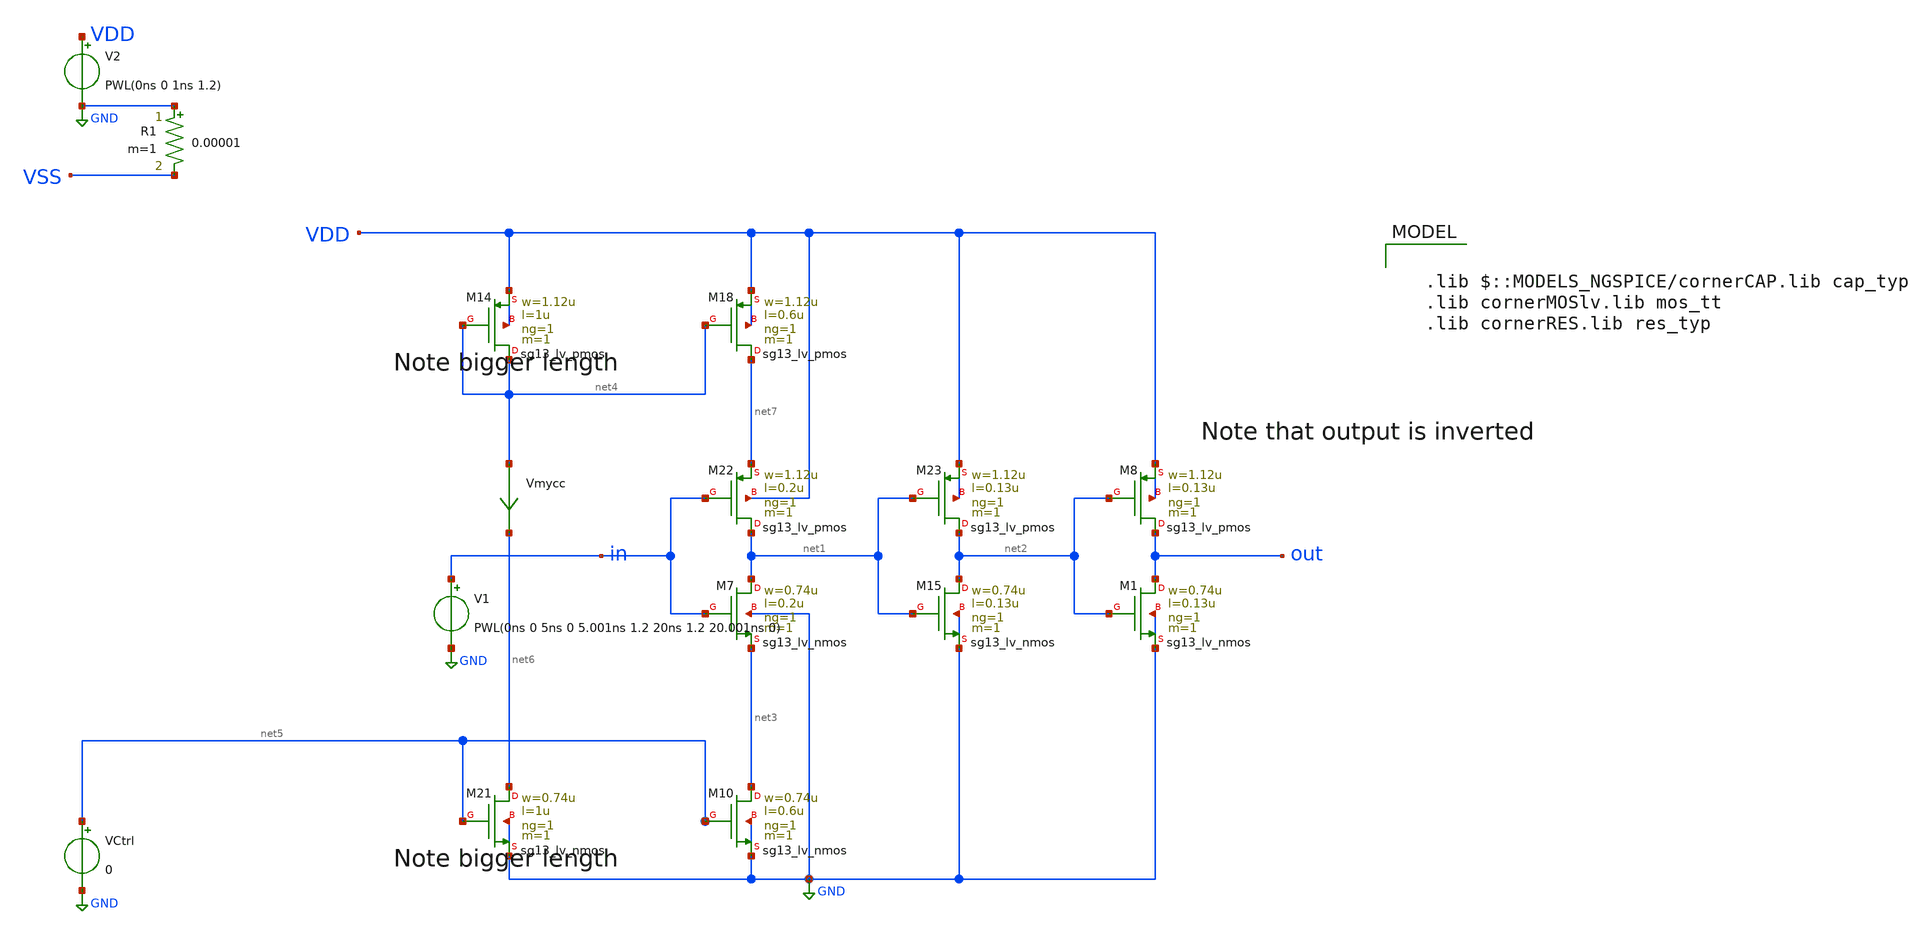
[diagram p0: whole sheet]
** sch_path: schematics/wip/delay_line_vary_voltage.sch
**.subckt delay_line_vary_voltage
XM7 net1 in net3 GND sg13_lv_nmos w=0.74u l=0.2u ng=1 m=1 mm_ok=1
XM10 net3 net5 GND GND sg13_lv_nmos w=0.74u l=0.6u ng=1 m=1 mm_ok=1
Vmycc net4 net6 0
.save i(vmycc)
XM18 net7 net4 VDD VDD sg13_lv_pmos w=1.12u l=0.6u ng=1 m=1 mm_ok=1
XM14 net4 net4 VDD VDD sg13_lv_pmos w=1.12u l=1u ng=1 m=1 mm_ok=1
XM15 net2 net1 GND GND sg13_lv_nmos w=0.74u l=0.13u ng=1 m=1 mm_ok=1
XM21 net6 net5 GND GND sg13_lv_nmos w=0.74u l=1u ng=1 m=1 mm_ok=1
XM22 net1 in net7 VDD sg13_lv_pmos w=1.12u l=0.2u ng=1 m=1 mm_ok=1
XM23 net2 net1 VDD VDD sg13_lv_pmos w=1.12u l=0.13u ng=1 m=1 mm_ok=1
V2 VDD GND PWL(0ns 0 1ns 1.2)
V1 in GND PWL(0ns 0 5ns 0 5.001ns 1.2 20ns 1.2 20.001ns 0)
R1 GND VSS 0.00001 m=1
VCtrl net5 GND 0
XM1 out net2 GND GND sg13_lv_nmos w=0.74u l=0.13u ng=1 m=1 mm_ok=1
XM8 out net2 VDD VDD sg13_lv_pmos w=1.12u l=0.13u ng=1 m=1 mm_ok=1
**** begin user architecture code

  .lib $::MODELS_NGSPICE/cornerCAP.lib cap_typ
  .lib cornerMOSlv.lib mos_tt
  .lib cornerRES.lib res_typ



.options temp=27
.include sg13g2_stdcell.spice
.control
  * 1. Define the sweep parameters
  let v_start = 0.40
  let v_stop = 1.0
  let v_step = 0.02
  let v_steps = (v_stop - v_start) / v_step + 1

  * 2. Create empty vectors to store our summary data
  let v_axis = unitvec(v_steps)
  let delay_results = unitvec(v_steps)
  let freq_results = unitvec(v_steps)
  let index = 0

  while index <= v_steps
    let v_act = v_start + index * v_step
    save all
    alter VCtrl v_act
    tran 5p 25n

    * Perform measurement
    * Please note that the output is inverted, so we detect FALLing edge
    meas tran tdiff TRIG v(in) VAL=0.6 RISE=1 TARG v(out) VAL=0.6 FALL=1


    let delay_results[index] = tdiff
    let freq_results[index] = 1/tdiff
    let v_axis[index] = v_act

    let v_act = v_act + v_step
    let index = index + 1


    write delay_line_vary_voltage.raw
  end

  * 4. Plot the results:
  plot delay_results vs v_axis title 'Delay vs Ctrl voltage' xlabel 'V (V)' ylabel 'Delay (s)'
  plot freq_results vs v_axis title 'Freq vs Ctrl voltage' xlabel 'V (V)' ylabel 'Frequency (Hz)'



.endc


**** end user architecture code
**.ends
.GLOBAL GND
.end
